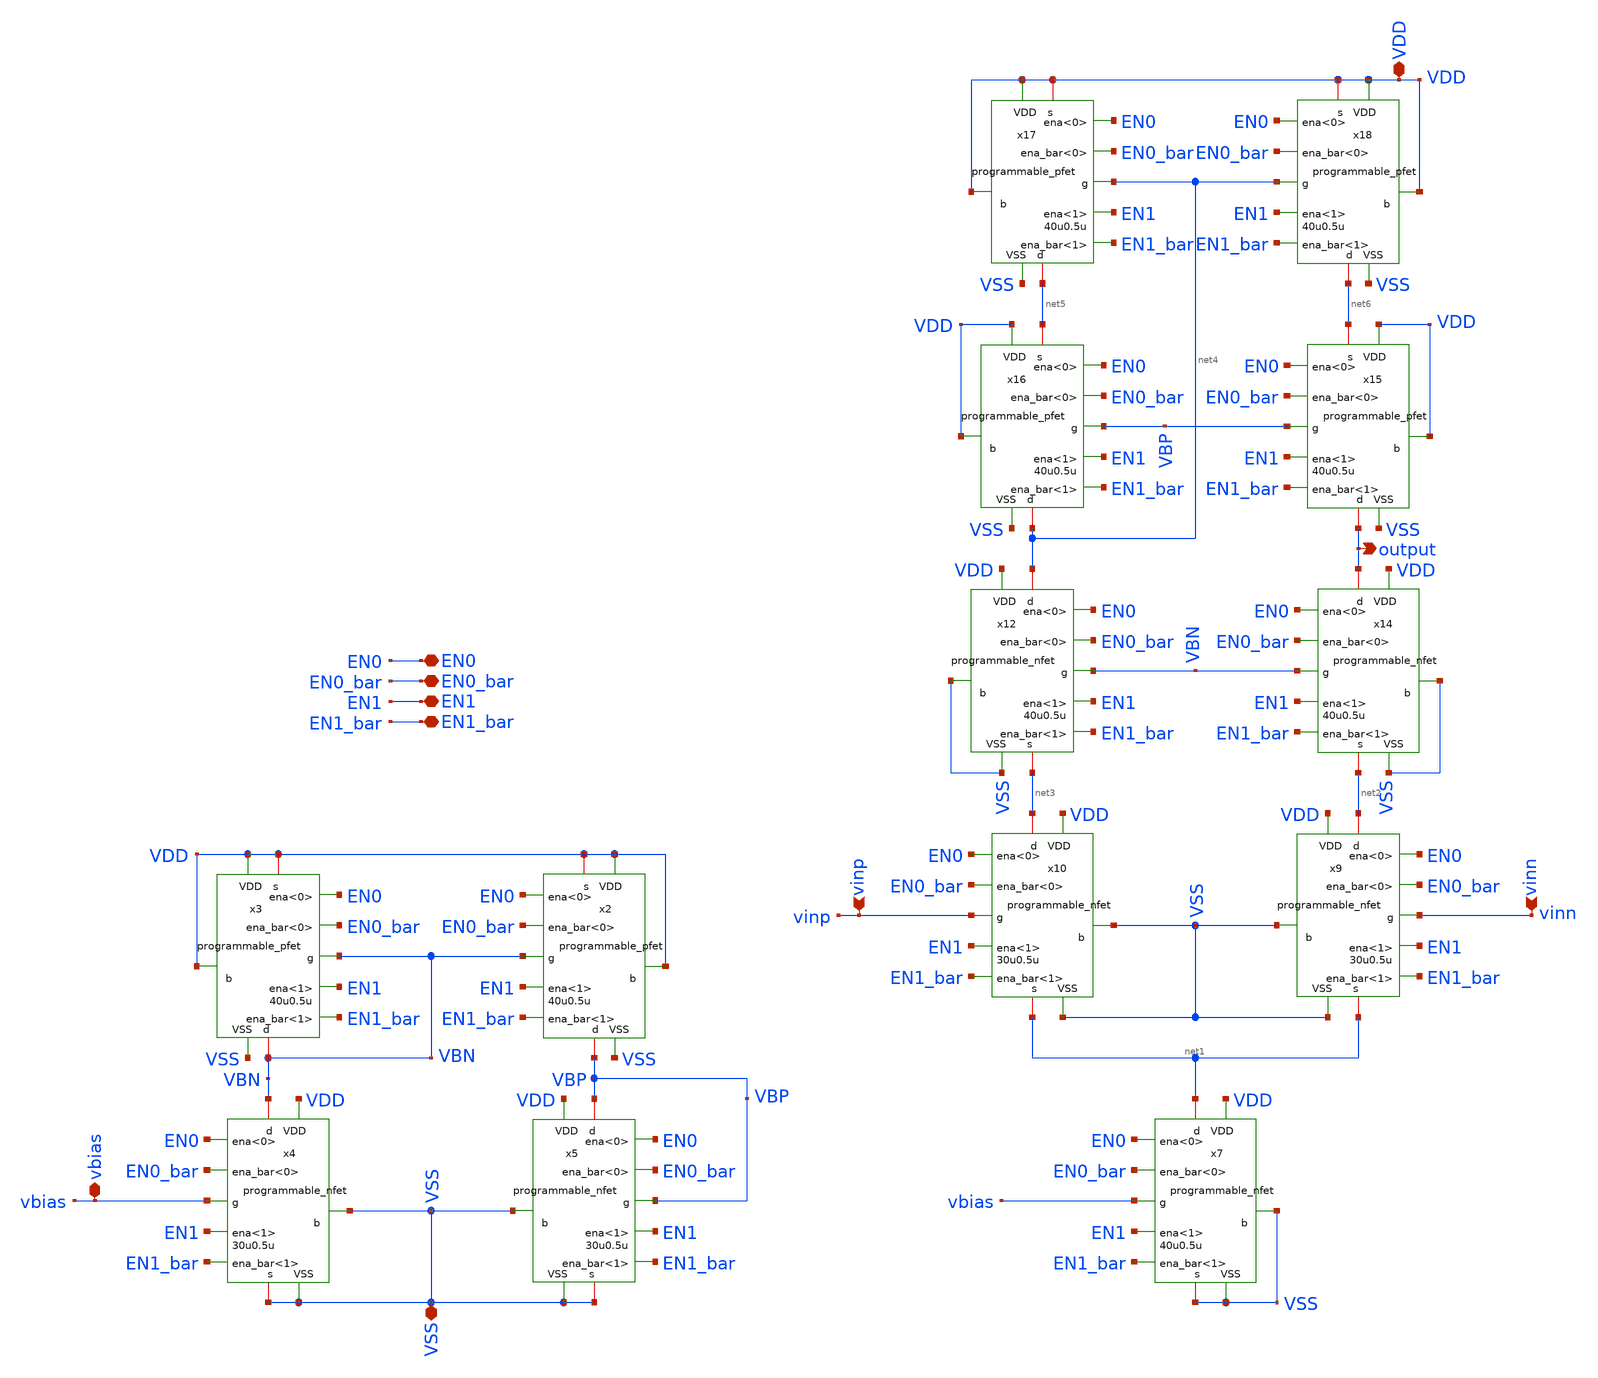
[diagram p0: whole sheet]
** sch_path: designs/libs/core_amps/ota_telescopic/programmable_telescopic_cascode.sch
**.subckt programmable_telescopic_cascode output vbias VDD EN0_bar EN1 EN0 EN1_bar VSS vinp vinn
*.opin output
*.iopin vbias
*.iopin VDD
*.iopin EN0_bar
*.iopin EN1
*.iopin EN0
*.iopin EN1_bar
*.iopin VSS
*.ipin vinp
*.ipin vinn
x2 VBP VDD VBN VDD EN0_bar VDD EN1_bar EN0 EN1 VSS programmable_pfet width=40u length=0.5u
x3 VBN VDD VBN VDD EN0_bar VDD EN1_bar EN0 EN1 VSS programmable_pfet width=40u length=0.5u
x5 VBP VSS VBP VSS EN0_bar VDD EN1_bar EN0 EN1 VSS programmable_nfet width=30u length=0.5u
x4 VBN VSS vbias VSS EN0_bar VDD EN1_bar EN0 EN1 VSS programmable_nfet width=30u length=0.5u
x7 net1 VSS vbias VSS EN0_bar VDD EN1_bar EN0 EN1 VSS programmable_nfet width=40u length=0.5u
x9 net2 VSS vinn net1 EN0_bar VDD EN1_bar EN0 EN1 VSS programmable_nfet width=30u length=0.5u
x10 net3 VSS vinp net1 EN0_bar VDD EN1_bar EN0 EN1 VSS programmable_nfet width=30u length=0.5u
x12 net4 VSS VBN net3 EN0_bar VDD EN1_bar EN0 EN1 VSS programmable_nfet width=40u length=0.5u
x14 output VSS VBN net2 EN0_bar VDD EN1_bar EN0 EN1 VSS programmable_nfet width=40u length=0.5u
x15 output VDD VBP net6 EN0_bar VDD EN1_bar EN0 EN1 VSS programmable_pfet width=40u length=0.5u
x16 net4 VDD VBP net5 EN0_bar VDD EN1_bar EN0 EN1 VSS programmable_pfet width=40u length=0.5u
x17 net5 VDD net4 VDD EN0_bar VDD EN1_bar EN0 EN1 VSS programmable_pfet width=40u length=0.5u
x18 net6 VDD net4 VDD EN0_bar VDD EN1_bar EN0 EN1 VSS programmable_pfet width=40u length=0.5u
**** begin user architecture code


.include /foss/pdks/gf180mcuD/libs.tech/ngspice/design.ngspice
.lib /foss/pdks/gf180mcuD/libs.tech/ngspice/sm141064.ngspice typical

**** end user architecture code
**.ends
.end
